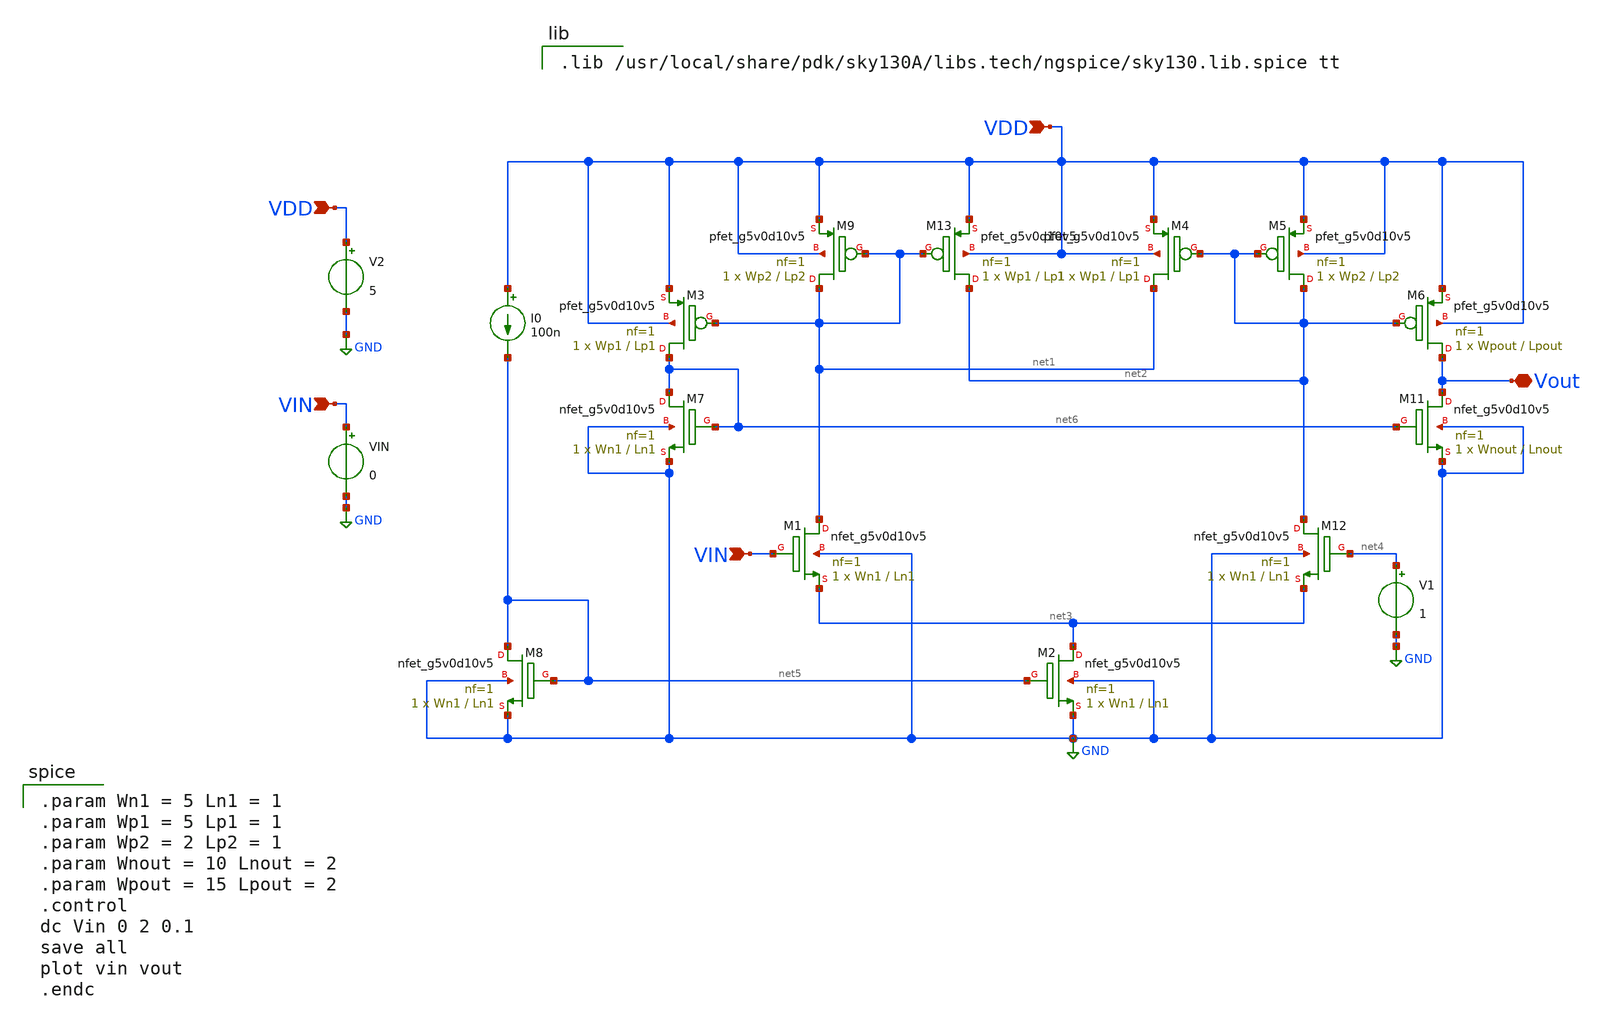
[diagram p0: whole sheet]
** sch_path: xschem/Comparador_completo.sch
**.subckt Comparador_completo VDD VDD Vout VIN VIN
*.ipin VDD
*.ipin VDD
*.iopin Vout
*.ipin VIN
*.ipin VIN
V1 net4 GND 1
V2 VDD GND 5
VIN VIN GND 0
I0 VDD net5 100n
XM3 net6 net1 VDD VDD sky130_fd_pr__pfet_g5v0d10v5 L=Lp1 W=Wp1 nf=1 ad='int((nf+1)/2) * W/nf * 0.29'
+ as='int((nf+2)/2) * W/nf * 0.29' pd='2*int((nf+1)/2) * (W/nf + 0.29)' ps='2*int((nf+2)/2) * (W/nf + 0.29)'
+ nrd='0.29 / W' nrs='0.29 / W' sa=0 sb=0 sd=0 mult=1 m=1
XM9 net1 net1 VDD VDD sky130_fd_pr__pfet_g5v0d10v5 L=Lp2 W=Wp2 nf=1 ad='int((nf+1)/2) * W/nf * 0.29'
+ as='int((nf+2)/2) * W/nf * 0.29' pd='2*int((nf+1)/2) * (W/nf + 0.29)' ps='2*int((nf+2)/2) * (W/nf + 0.29)'
+ nrd='0.29 / W' nrs='0.29 / W' sa=0 sb=0 sd=0 mult=1 m=1
XM13 net2 net1 VDD VDD sky130_fd_pr__pfet_g5v0d10v5 L=Lp1 W=Wp1 nf=1 ad='int((nf+1)/2) * W/nf * 0.29'
+ as='int((nf+2)/2) * W/nf * 0.29' pd='2*int((nf+1)/2) * (W/nf + 0.29)' ps='2*int((nf+2)/2) * (W/nf + 0.29)'
+ nrd='0.29 / W' nrs='0.29 / W' sa=0 sb=0 sd=0 mult=1 m=1
XM4 net1 net2 VDD VDD sky130_fd_pr__pfet_g5v0d10v5 L=Lp1 W=Wp1 nf=1 ad='int((nf+1)/2) * W/nf * 0.29'
+ as='int((nf+2)/2) * W/nf * 0.29' pd='2*int((nf+1)/2) * (W/nf + 0.29)' ps='2*int((nf+2)/2) * (W/nf + 0.29)'
+ nrd='0.29 / W' nrs='0.29 / W' sa=0 sb=0 sd=0 mult=1 m=1
XM5 net2 net2 VDD VDD sky130_fd_pr__pfet_g5v0d10v5 L=Lp2 W=Wp2 nf=1 ad='int((nf+1)/2) * W/nf * 0.29'
+ as='int((nf+2)/2) * W/nf * 0.29' pd='2*int((nf+1)/2) * (W/nf + 0.29)' ps='2*int((nf+2)/2) * (W/nf + 0.29)'
+ nrd='0.29 / W' nrs='0.29 / W' sa=0 sb=0 sd=0 mult=1 m=1
XM6 Vout net2 VDD VDD sky130_fd_pr__pfet_g5v0d10v5 L=Lpout W=Wpout nf=1 ad='int((nf+1)/2) * W/nf * 0.29'
+ as='int((nf+2)/2) * W/nf * 0.29' pd='2*int((nf+1)/2) * (W/nf + 0.29)' ps='2*int((nf+2)/2) * (W/nf + 0.29)'
+ nrd='0.29 / W' nrs='0.29 / W' sa=0 sb=0 sd=0 mult=1 m=1
XM11 Vout net6 GND GND sky130_fd_pr__nfet_g5v0d10v5 L=Lnout W=Wnout nf=1 ad='int((nf+1)/2) * W/nf * 0.29'
+ as='int((nf+2)/2) * W/nf * 0.29' pd='2*int((nf+1)/2) * (W/nf + 0.29)' ps='2*int((nf+2)/2) * (W/nf + 0.29)'
+ nrd='0.29 / W' nrs='0.29 / W' sa=0 sb=0 sd=0 mult=1 m=1
XM12 net2 net4 net3 GND sky130_fd_pr__nfet_g5v0d10v5 L=Ln1 W=Wn1 nf=1 ad='int((nf+1)/2) * W/nf * 0.29'
+ as='int((nf+2)/2) * W/nf * 0.29' pd='2*int((nf+1)/2) * (W/nf + 0.29)' ps='2*int((nf+2)/2) * (W/nf + 0.29)'
+ nrd='0.29 / W' nrs='0.29 / W' sa=0 sb=0 sd=0 mult=1 m=1
XM2 net3 net5 GND GND sky130_fd_pr__nfet_g5v0d10v5 L=Ln1 W=Wn1 nf=1 ad='int((nf+1)/2) * W/nf * 0.29'
+ as='int((nf+2)/2) * W/nf * 0.29' pd='2*int((nf+1)/2) * (W/nf + 0.29)' ps='2*int((nf+2)/2) * (W/nf + 0.29)'
+ nrd='0.29 / W' nrs='0.29 / W' sa=0 sb=0 sd=0 mult=1 m=1
XM1 net1 VIN net3 GND sky130_fd_pr__nfet_g5v0d10v5 L=Ln1 W=Wn1 nf=1 ad='int((nf+1)/2) * W/nf * 0.29'
+ as='int((nf+2)/2) * W/nf * 0.29' pd='2*int((nf+1)/2) * (W/nf + 0.29)' ps='2*int((nf+2)/2) * (W/nf + 0.29)'
+ nrd='0.29 / W' nrs='0.29 / W' sa=0 sb=0 sd=0 mult=1 m=1
XM7 net6 net6 GND GND sky130_fd_pr__nfet_g5v0d10v5 L=Ln1 W=Wn1 nf=1 ad='int((nf+1)/2) * W/nf * 0.29'
+ as='int((nf+2)/2) * W/nf * 0.29' pd='2*int((nf+1)/2) * (W/nf + 0.29)' ps='2*int((nf+2)/2) * (W/nf + 0.29)'
+ nrd='0.29 / W' nrs='0.29 / W' sa=0 sb=0 sd=0 mult=1 m=1
XM8 net5 net5 GND GND sky130_fd_pr__nfet_g5v0d10v5 L=Ln1 W=Wn1 nf=1 ad='int((nf+1)/2) * W/nf * 0.29'
+ as='int((nf+2)/2) * W/nf * 0.29' pd='2*int((nf+1)/2) * (W/nf + 0.29)' ps='2*int((nf+2)/2) * (W/nf + 0.29)'
+ nrd='0.29 / W' nrs='0.29 / W' sa=0 sb=0 sd=0 mult=1 m=1
**** begin user architecture code

.param Wn1 = 5 Ln1 = 1
.param Wp1 = 5 Lp1 = 1
.param Wp2 = 2 Lp2 = 1
.param Wnout = 10 Lnout = 2
.param Wpout = 15 Lpout = 2
.control
dc Vin 0 2 0.1
save all
plot vin vout
.endc


.lib /usr/local/share/pdk/sky130A/libs.tech/ngspice/sky130.lib.spice tt

**** end user architecture code
**.ends
.GLOBAL GND
.end
